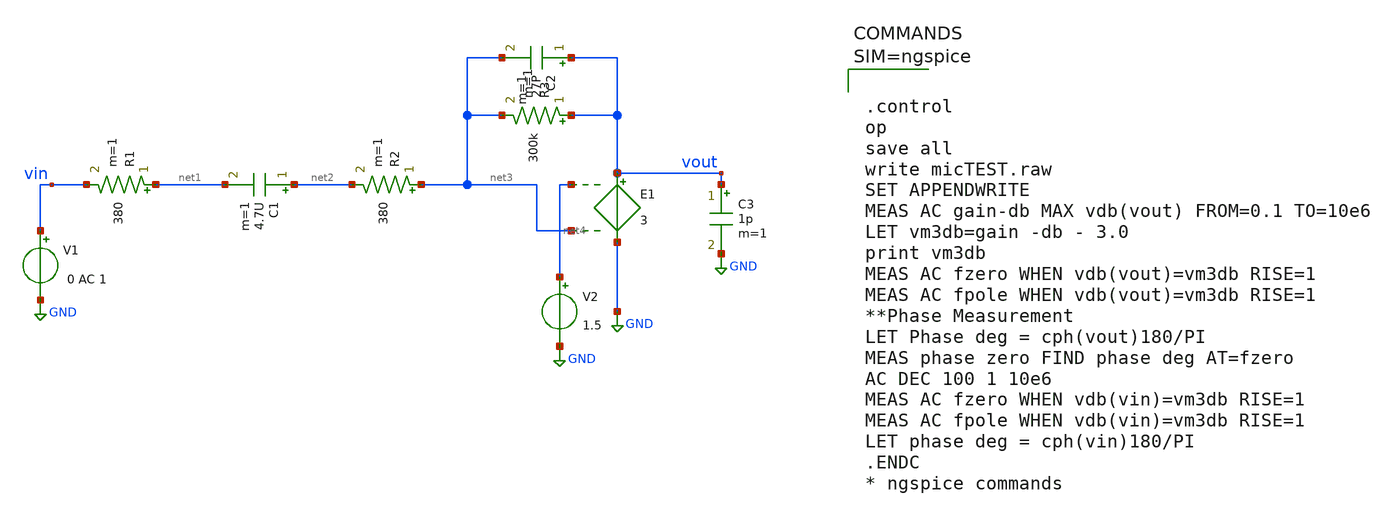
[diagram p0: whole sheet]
** sch_path: xschem/untitled-1.sch
**.subckt untitled-1
R1 net1 vin 380 m=1
C1 net2 net1 4.7U m=1
R2 net3 net2 380 m=1
C2 vout net3 27P m=1
R3 vout net3 300k m=1
E1 vout GND net4 net3 3
C3 vout GND 1p m=1
V2 net4 GND 1.5
V1 vin GND 0 AC 1
**** begin user architecture code



.control
op
save all
write micTEST.raw
SET APPENDWRITE
MEAS AC gain-db MAX vdb(vout) FROM=0.1 TO=10e6
LET vm3db=gain -db - 3.0
print vm3db
MEAS AC fzero WHEN vdb(vout)=vm3db RISE=1
MEAS AC fpole WHEN vdb(vout)=vm3db RISE=1
**Phase Measurement
LET Phase deg = cph(vout)180/PI
MEAS phase zero FIND phase deg AT=fzero
AC DEC 100 1 10e6
MEAS AC fzero WHEN vdb(vin)=vm3db RISE=1
MEAS AC fpole WHEN vdb(vin)=vm3db RISE=1
LET phase deg = cph(vin)180/PI
.ENDC
* ngspice commands



**** end user architecture code
**.ends
.GLOBAL GND
.end
